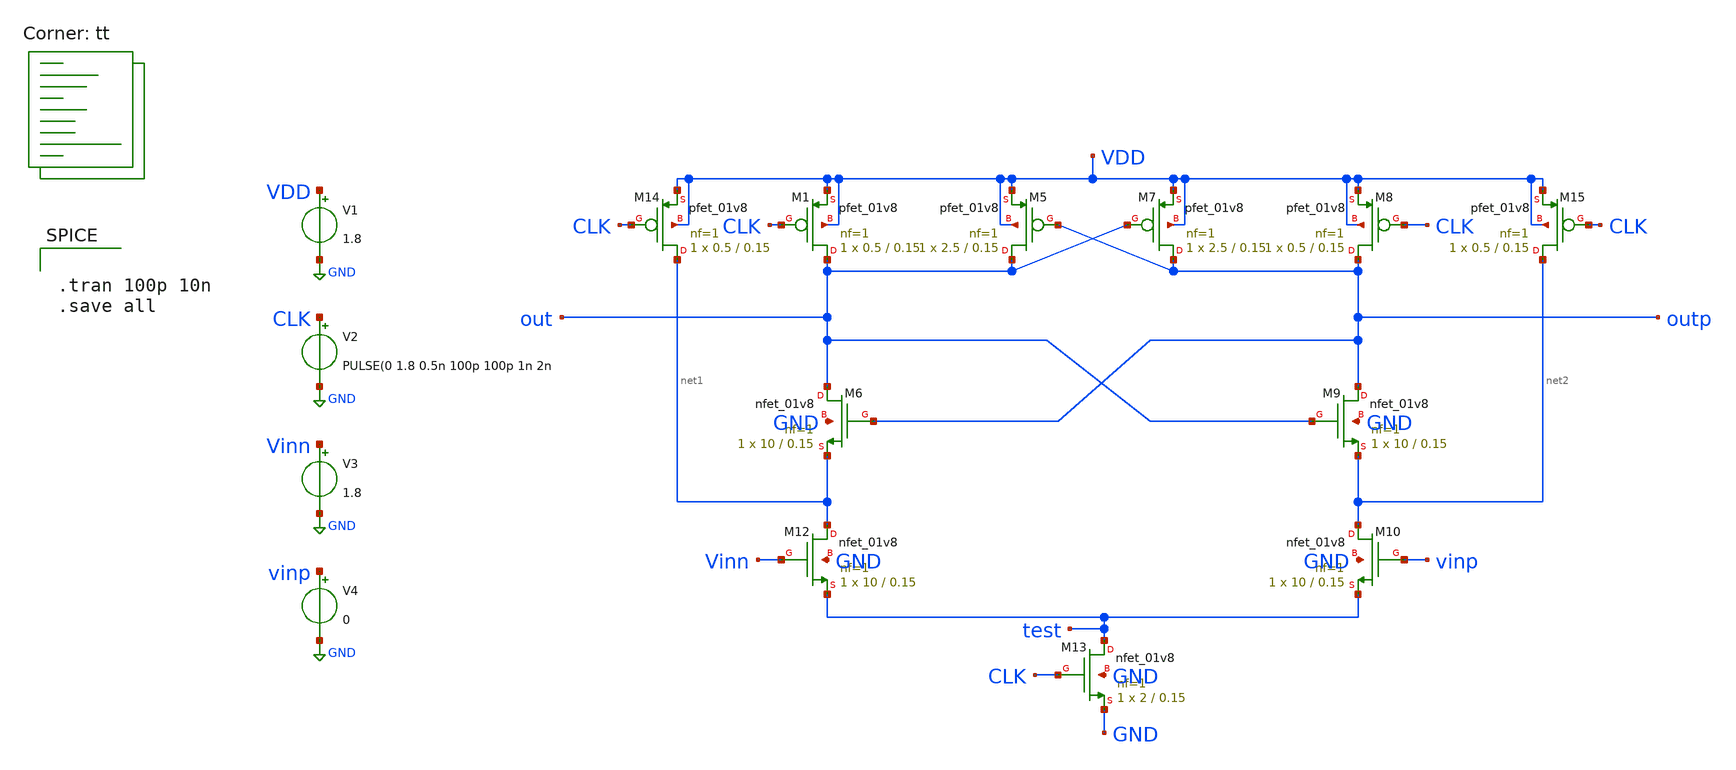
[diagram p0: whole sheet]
** sch_path: xschem/vault/CT.sch
**.subckt CT
V2 CLK GND PULSE(0 1.8 0.5n 100p 100p 1n 2n
V1 VDD GND 1.8
V3 Vinn GND 1.8
V4 vinp GND 0
XM12 net1 Vinn test GND sky130_fd_pr__nfet_01v8 L=0.15 W=10 nf=1 ad='int((nf+1)/2) * W/nf * 0.29' as='int((nf+2)/2) * W/nf * 0.29'
+ pd='2*int((nf+1)/2) * (W/nf + 0.29)' ps='2*int((nf+2)/2) * (W/nf + 0.29)' nrd='0.29 / W' nrs='0.29 / W'
+ sa=0 sb=0 sd=0 mult=1 m=1
XM5 out outp VDD VDD sky130_fd_pr__pfet_01v8 L=0.15 W=2.5 nf=1 ad='int((nf+1)/2) * W/nf * 0.29' as='int((nf+2)/2) * W/nf * 0.29'
+ pd='2*int((nf+1)/2) * (W/nf + 0.29)' ps='2*int((nf+2)/2) * (W/nf + 0.29)' nrd='0.29 / W' nrs='0.29 / W'
+ sa=0 sb=0 sd=0 mult=1 m=1
XM6 out outp net1 GND sky130_fd_pr__nfet_01v8 L=0.15 W=10 nf=1 ad='int((nf+1)/2) * W/nf * 0.29' as='int((nf+2)/2) * W/nf * 0.29'
+ pd='2*int((nf+1)/2) * (W/nf + 0.29)' ps='2*int((nf+2)/2) * (W/nf + 0.29)' nrd='0.29 / W' nrs='0.29 / W'
+ sa=0 sb=0 sd=0 mult=1 m=1
XM7 outp out VDD VDD sky130_fd_pr__pfet_01v8 L=0.15 W=2.5 nf=1 ad='int((nf+1)/2) * W/nf * 0.29' as='int((nf+2)/2) * W/nf * 0.29'
+ pd='2*int((nf+1)/2) * (W/nf + 0.29)' ps='2*int((nf+2)/2) * (W/nf + 0.29)' nrd='0.29 / W' nrs='0.29 / W'
+ sa=0 sb=0 sd=0 mult=1 m=1
XM8 outp CLK VDD VDD sky130_fd_pr__pfet_01v8 L=0.15 W=0.5 nf=1 ad='int((nf+1)/2) * W/nf * 0.29' as='int((nf+2)/2) * W/nf * 0.29'
+ pd='2*int((nf+1)/2) * (W/nf + 0.29)' ps='2*int((nf+2)/2) * (W/nf + 0.29)' nrd='0.29 / W' nrs='0.29 / W'
+ sa=0 sb=0 sd=0 mult=1 m=1
XM9 outp out net2 GND sky130_fd_pr__nfet_01v8 L=0.15 W=10 nf=1 ad='int((nf+1)/2) * W/nf * 0.29' as='int((nf+2)/2) * W/nf * 0.29'
+ pd='2*int((nf+1)/2) * (W/nf + 0.29)' ps='2*int((nf+2)/2) * (W/nf + 0.29)' nrd='0.29 / W' nrs='0.29 / W'
+ sa=0 sb=0 sd=0 mult=1 m=1
XM10 net2 vinp test GND sky130_fd_pr__nfet_01v8 L=0.15 W=10 nf=1 ad='int((nf+1)/2) * W/nf * 0.29' as='int((nf+2)/2) * W/nf * 0.29'
+ pd='2*int((nf+1)/2) * (W/nf + 0.29)' ps='2*int((nf+2)/2) * (W/nf + 0.29)' nrd='0.29 / W' nrs='0.29 / W'
+ sa=0 sb=0 sd=0 mult=1 m=1
XM13 test CLK GND GND sky130_fd_pr__nfet_01v8 L=0.15 W=2 nf=1 ad='int((nf+1)/2) * W/nf * 0.29' as='int((nf+2)/2) * W/nf * 0.29'
+ pd='2*int((nf+1)/2) * (W/nf + 0.29)' ps='2*int((nf+2)/2) * (W/nf + 0.29)' nrd='0.29 / W' nrs='0.29 / W'
+ sa=0 sb=0 sd=0 mult=1 m=1
XM14 net1 CLK VDD VDD sky130_fd_pr__pfet_01v8 L=0.15 W=0.5 nf=1 ad='int((nf+1)/2) * W/nf * 0.29' as='int((nf+2)/2) * W/nf * 0.29'
+ pd='2*int((nf+1)/2) * (W/nf + 0.29)' ps='2*int((nf+2)/2) * (W/nf + 0.29)' nrd='0.29 / W' nrs='0.29 / W'
+ sa=0 sb=0 sd=0 mult=1 m=1
XM15 net2 CLK VDD VDD sky130_fd_pr__pfet_01v8 L=0.15 W=0.5 nf=1 ad='int((nf+1)/2) * W/nf * 0.29' as='int((nf+2)/2) * W/nf * 0.29'
+ pd='2*int((nf+1)/2) * (W/nf + 0.29)' ps='2*int((nf+2)/2) * (W/nf + 0.29)' nrd='0.29 / W' nrs='0.29 / W'
+ sa=0 sb=0 sd=0 mult=1 m=1
XM1 out CLK VDD VDD sky130_fd_pr__pfet_01v8 L=0.15 W=0.5 nf=1 ad='int((nf+1)/2) * W/nf * 0.29' as='int((nf+2)/2) * W/nf * 0.29'
+ pd='2*int((nf+1)/2) * (W/nf + 0.29)' ps='2*int((nf+2)/2) * (W/nf + 0.29)' nrd='0.29 / W' nrs='0.29 / W'
+ sa=0 sb=0 sd=0 mult=1 m=1
**** begin user architecture code
.lib $::SKYWATER_MODELS/sky130.lib.spice tt


.tran 100p 10n
.save all


**** end user architecture code
**.ends
.GLOBAL GND
.end
